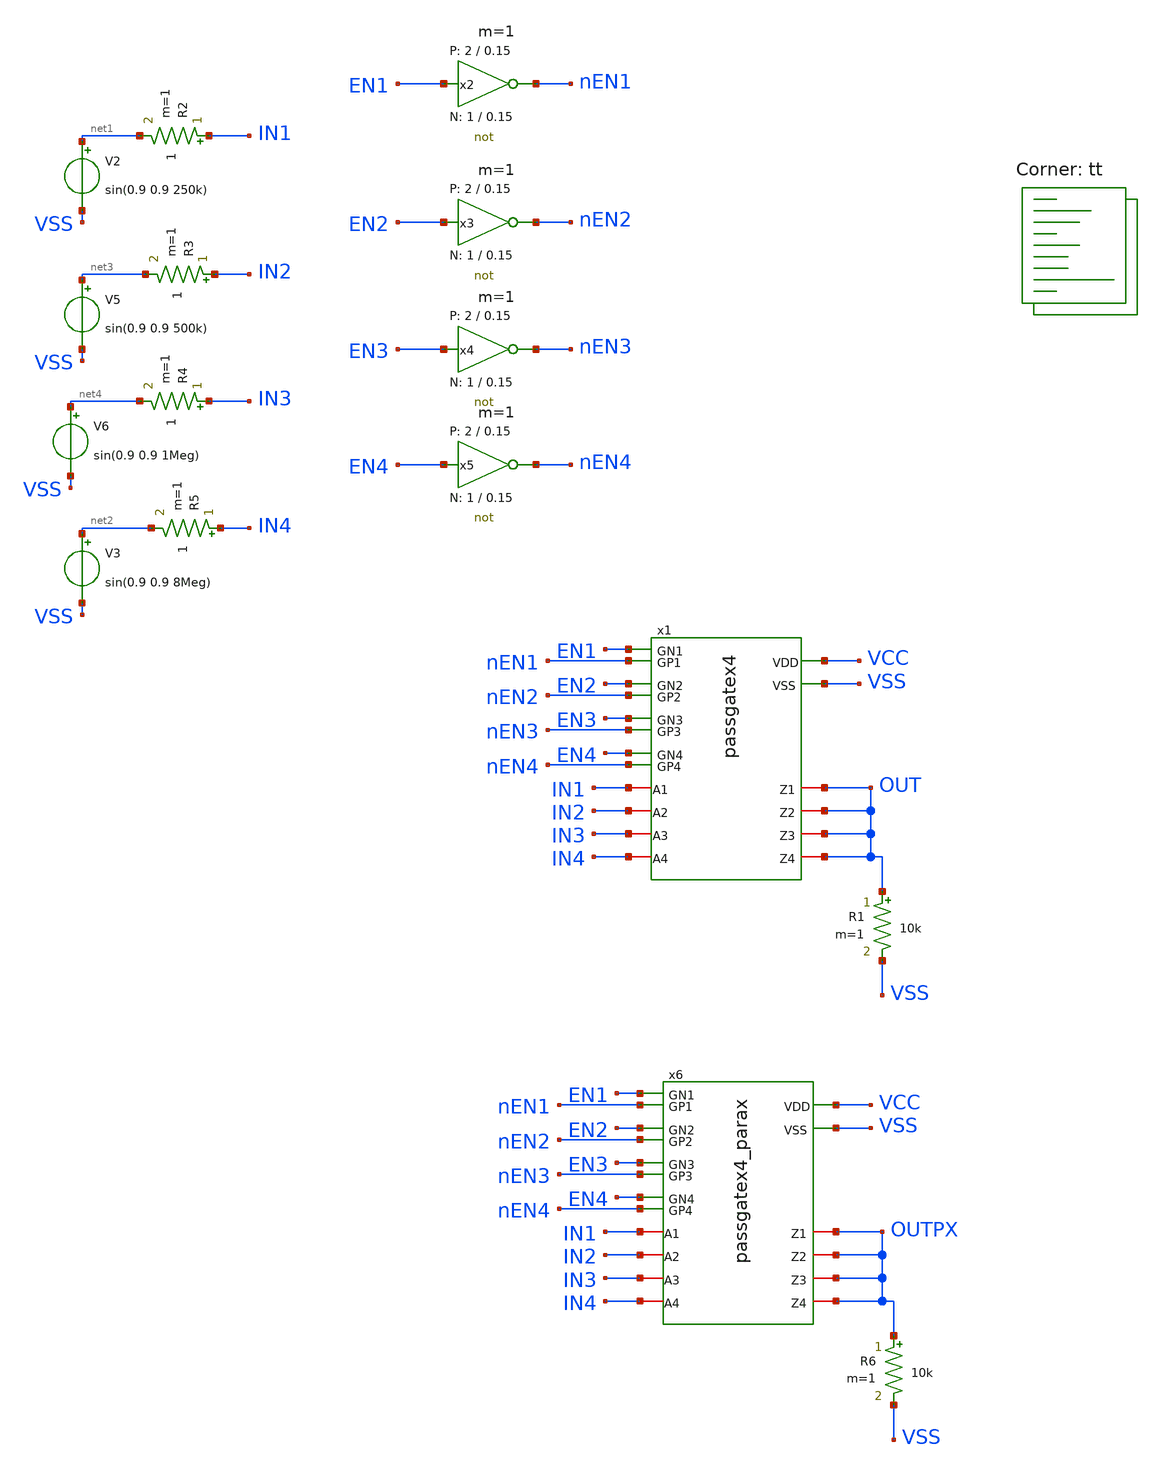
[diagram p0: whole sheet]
** sch_path: xschem/tb_passgatex4.sch
* StefanSchippers/xschem_sky130/sky130_tests/not.sch:
* Copyright 2021 Stefan Frederik Schippers
* Licensed under the Apache License, Version 2.0 (the "License");
**.subckt tb_passgatex4
x1 IN1 EN1 nEN1 OUT IN2 EN2 nEN2 OUT IN3 EN3 nEN3 OUT IN4 EN4 nEN4 OUT VCC VSS passgatex4
x2 nEN1 EN1 VCC VSS not W_N=1 L_N=0.15 W_P=2 L_P=0.15 m=1
V2 net1 VSS sin(0.9 0.9 250k)
x3 nEN2 EN2 VCC VSS not W_N=1 L_N=0.15 W_P=2 L_P=0.15 m=1
x4 nEN3 EN3 VCC VSS not W_N=1 L_N=0.15 W_P=2 L_P=0.15 m=1
x5 nEN4 EN4 VCC VSS not W_N=1 L_N=0.15 W_P=2 L_P=0.15 m=1
V3 net2 VSS sin(0.9 0.9 8Meg)
V5 net3 VSS sin(0.9 0.9 500k)
V6 net4 VSS sin(0.9 0.9 1Meg)
R1 OUT VSS 10k m=1
R2 IN1 net1 1 m=1
R3 IN2 net3 1 m=1
R4 IN3 net4 1 m=1
R5 IN4 net2 1 m=1
x6 IN1 EN1 nEN1 OUTPX IN2 EN2 nEN2 OUTPX IN3 EN3 nEN3 OUTPX IN4 EN4 nEN4 OUTPX VCC VSS
+ passgatex4_parax
R6 OUTPX VSS 10k m=1
**** begin user architecture code
.lib $::SKYWATER_MODELS/sky130.lib.spice tt
**** end user architecture code
**.ends

* expanding   symbol:  passgatex4.sym # of pins=18
** sym_path: xschem/passgatex4.sym
** sch_path: xschem/passgatex4.sch
.subckt passgatex4 A1 GN1 GP1 Z1 A2 GN2 GP2 Z2 A3 GN3 GP3 Z3 A4 GN4 GP4 Z4 VDD VSS
*.ipin VDD
*.ipin VSS
*.ipin GP1
*.ipin GN1
*.iopin A1
*.iopin Z1
*.ipin GP2
*.ipin GN2
*.iopin A2
*.iopin Z2
*.ipin GP3
*.ipin GN3
*.iopin A3
*.iopin Z3
*.ipin GP4
*.ipin GN4
*.iopin A4
*.iopin Z4
x1 A1 GN1 GP1 Z1 VDD VSS passgate
x2 A2 GN2 GP2 Z2 VDD VSS passgate
x3 A3 GN3 GP3 Z3 VDD VSS passgate
x4 A4 GN4 GP4 Z4 VDD VSS passgate
.ends


* expanding   symbol:  sky130_tests/not.sym # of pins=2
** sym_path: sky130_tests/not.sym
** sch_path: sky130_tests/not.sch
.subckt not y a VCCPIN VSSPIN     W_N=1 L_N=0.15 W_P=2 L_P=0.15
*.opin y
*.ipin a
XM1 DN a VSSPIN VSSPIN sky130_fd_pr__nfet_01v8 L=L_N W=W_N nf=1 ad='int((1 + 1)/2) * W_N / 1 * 0.29'
+ as='int((1 + 2)/2) * W_N / 1 * 0.29' pd='2*int((1 + 1)/2) * (W_N / 1 + 0.29)' ps='2*int((1 + 2)/2) * (W_N / 1 + 0.29)'
+ nrd='0.29 / W_N ' nrs='0.29 / W_N ' sa=0 sb=0 sd=0 mult=1 m=1
XM2 DP a VCCPIN VCCPIN sky130_fd_pr__pfet_01v8 L=L_P W=W_P nf=1 ad='int((nf+1)/2) * W/nf * 0.29' as='int((nf+2)/2) * W/nf * 0.29'
+ pd='2*int((nf+1)/2) * (W/nf + 0.29)' ps='2*int((nf+2)/2) * (W/nf + 0.29)' nrd='0.29 / W' nrs='0.29 / W'
+ sa=0 sb=0 sd=0 mult=1 m=1
Vmeas DP y 0
.save i(vmeas)
Vmeas1 y DN 0
.save i(vmeas1)
.save v(dp)
.save v(dn)
.ends


* expanding   symbol:  passgatex4_parax.sym # of pins=18
** sym_path: xschem/passgatex4.sym
.include [file normalize extracted/passgatex4_parax.spice]

* expanding   symbol:  passgate.sym # of pins=6
** sym_path: xschem/passgate.sym
** sch_path: xschem/passgate.sch
.subckt passgate A GN GP Z VDD VSS
*.ipin GN
*.ipin VDD
*.ipin VSS
*.ipin GP
*.iopin A
*.iopin Z
XM1 Z GN A VSS sky130_fd_pr__nfet_01v8_lvt L=0.35 W=8 nf=1 ad='int((nf+1)/2) * W/nf * 0.29' as='int((nf+2)/2) * W/nf * 0.29'
+ pd='2*int((nf+1)/2) * (W/nf + 0.29)' ps='2*int((nf+2)/2) * (W/nf + 0.29)' nrd='0.29 / W' nrs='0.29 / W'
+ sa=0 sb=0 sd=0 mult=2 m=2
XM3 Z GP A VDD sky130_fd_pr__pfet_01v8_lvt L=0.35 W=10 nf=1 ad='int((nf+1)/2) * W/nf * 0.29' as='int((nf+2)/2) * W/nf * 0.29'
+ pd='2*int((nf+1)/2) * (W/nf + 0.29)' ps='2*int((nf+2)/2) * (W/nf + 0.29)' nrd='0.29 / W' nrs='0.29 / W'
+ sa=0 sb=0 sd=0 mult=2 m=2
.ends

**** begin user architecture code


* ngspice commands
* .options savecurrents
.param VCC = 1.8
.param SRCRES = 1k
.include stimuli_tb_passgatex4.cir
.control
save all
op
write tb_passgatex4.raw
set appendwrite
tran 10n 50u
write tb_passgatex4.raw
quit 0
.endc



**** end user architecture code
.end
